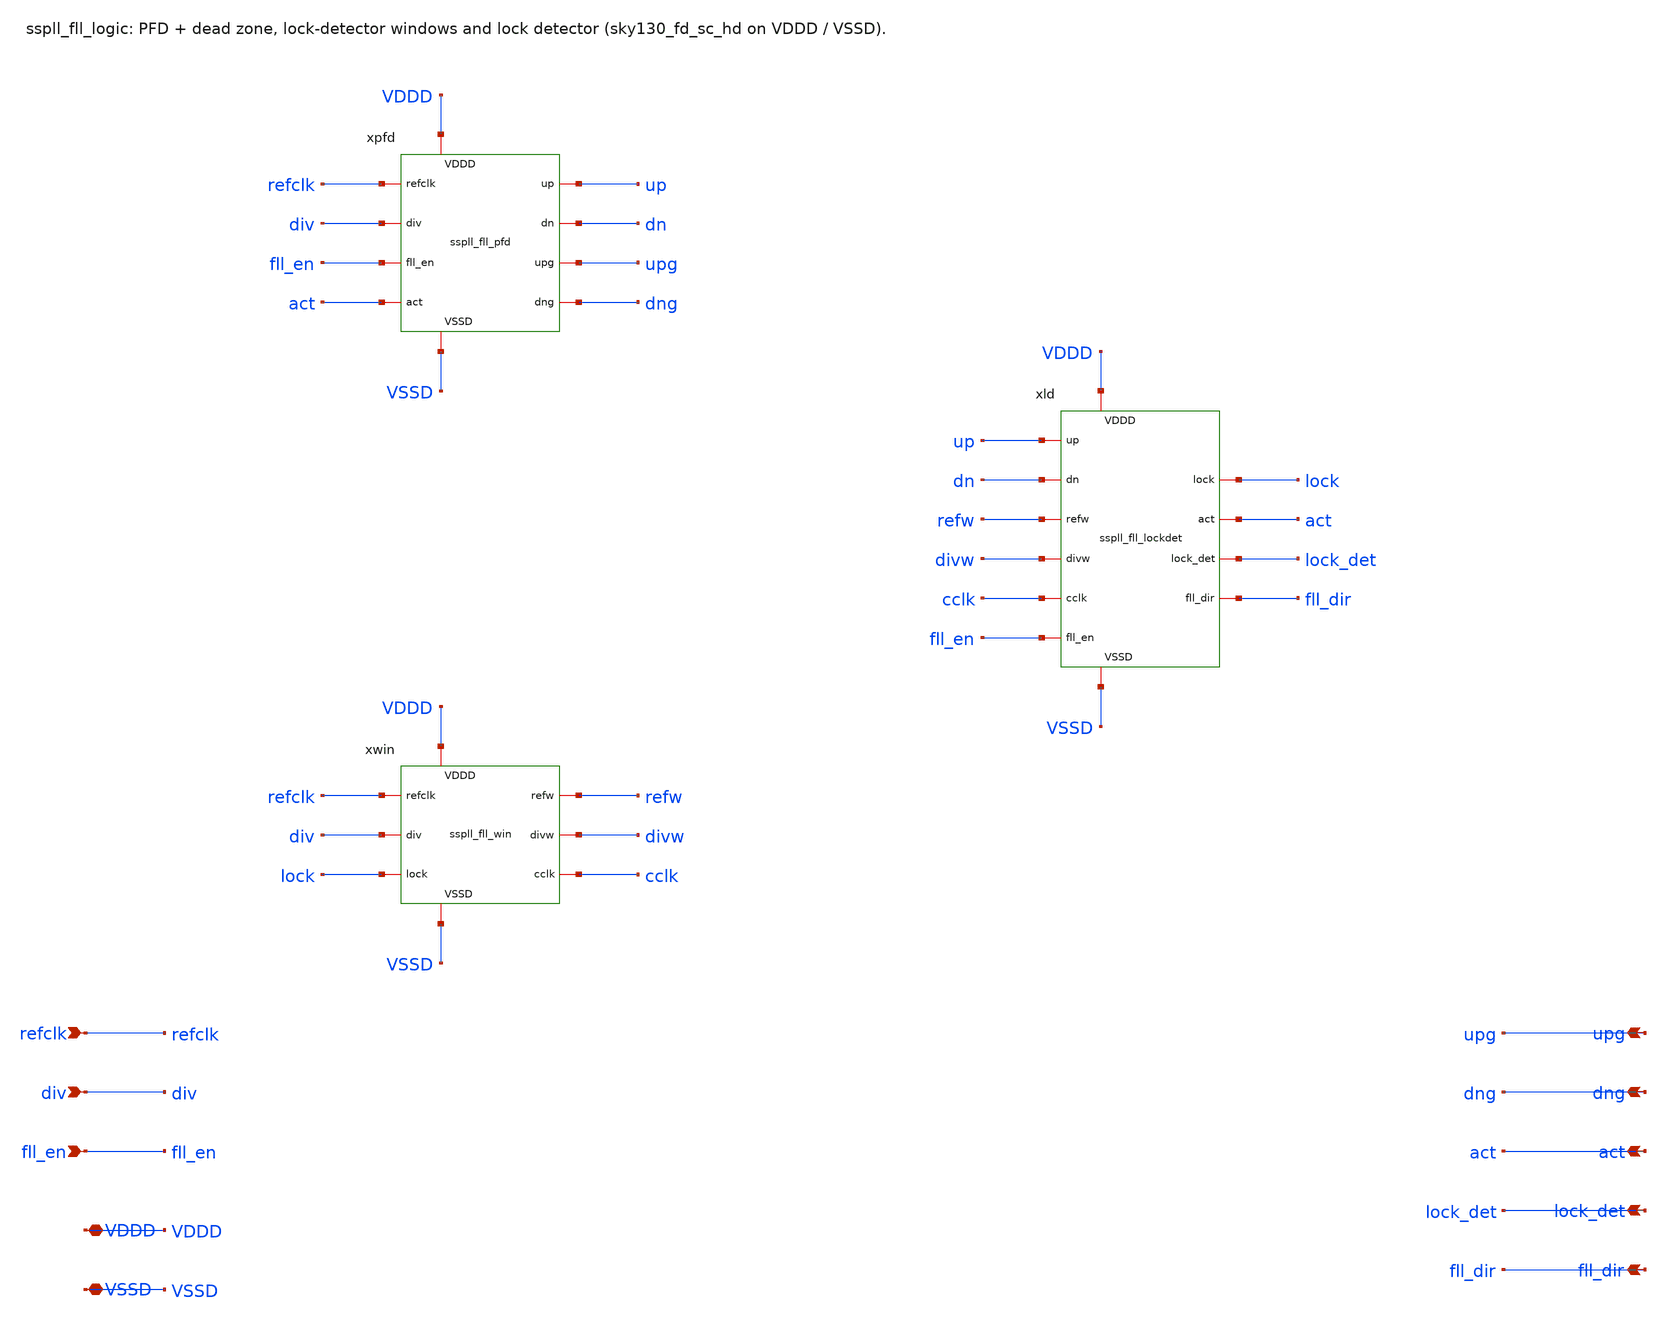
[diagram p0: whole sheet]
** sch_path: xschem/fll_hv/sspll_fll_logic.sch
**.subckt sspll_fll_logic refclk div fll_en upg dng act lock_det fll_dir VDDD VSSD
*.ipin refclk
*.ipin div
*.ipin fll_en
*.opin upg
*.opin dng
*.opin act
*.opin lock_det
*.opin fll_dir
*.iopin VDDD
*.iopin VSSD
xpfd refclk div fll_en act up dn upg dng VDDD VSSD sspll_fll_pfd
xwin refclk div lock refw divw cclk VDDD VSSD sspll_fll_win
xld up dn refw divw cclk fll_en lock act lock_det fll_dir VDDD VSSD sspll_fll_lockdet
**.ends

* expanding   symbol:  sspll_fll_pfd.sym # of pins=10
** sym_path: xschem/fll_hv/sspll_fll_pfd.sym
** sch_path: xschem/fll_hv/sspll_fll_pfd.sch
.subckt sspll_fll_pfd refclk div fll_en act up dn upg dng VDDD VSSD
*.ipin refclk
*.ipin div
*.ipin fll_en
*.ipin act
*.opin up
*.opin dn
*.opin upg
*.opin dng
*.iopin VDDD
*.iopin VSSD
xfu refclk VDDD rb VSSD VSSD VDDD VDDD up sky130_fd_sc_hd__dfrtp_1
xfd div VDDD rb VSSD VSSD VDDD VDDD dn sky130_fd_sc_hd__dfrtp_1
xrn up dn VSSD VSSD VDDD VDDD net1 sky130_fd_sc_hd__nand2_1
xrd net1 VSSD VSSD VDDD VDDD net2 sky130_fd_sc_hd__buf_1
xre net2 fll_en VSSD VSSD VDDD VDDD rb sky130_fd_sc_hd__and2_1
xzu1 up VSSD VSSD VDDD VDDD net3 sky130_fd_sc_hd__clkdlybuf4s25_1
xzu2 net3 VSSD VSSD VDDD VDDD net4 sky130_fd_sc_hd__buf_1
xgu up net4 act VSSD VSSD VDDD VDDD upg sky130_fd_sc_hd__and3_1
xzd1 dn VSSD VSSD VDDD VDDD net5 sky130_fd_sc_hd__clkdlybuf4s25_1
xzd2 net5 VSSD VSSD VDDD VDDD net6 sky130_fd_sc_hd__buf_1
xgd dn net6 act VSSD VSSD VDDD VDDD dng sky130_fd_sc_hd__and3_1
.ends


* expanding   symbol:  sspll_fll_win.sym # of pins=8
** sym_path: xschem/fll_hv/sspll_fll_win.sym
** sch_path: xschem/fll_hv/sspll_fll_win.sch
.subckt sspll_fll_win refclk div lock refw divw cclk VDDD VSSD
*.ipin refclk
*.ipin div
*.ipin lock
*.opin refw
*.opin divw
*.opin cclk
*.iopin VDDD
*.iopin VSSD
xwr1 refclk VSSD VSSD VDDD VDDD net1 sky130_fd_sc_hd__clkdlybuf4s50_1
xwr2 net1 VSSD VSSD VDDD VDDD net2 sky130_fd_sc_hd__clkdlybuf4s50_1
xwr3 net2 VSSD VSSD VDDD VDDD r3 sky130_fd_sc_hd__clkdlybuf4s50_1
xwr4 r3 VSSD VSSD VDDD VDDD net3 sky130_fd_sc_hd__clkdlybuf4s50_1
xwr5 net3 VSSD VSSD VDDD VDDD net4 sky130_fd_sc_hd__clkdlybuf4s50_1
xwr6 net4 VSSD VSSD VDDD VDDD net5 sky130_fd_sc_hd__clkdlybuf4s50_1
xwr7 net5 VSSD VSSD VDDD VDDD r7 sky130_fd_sc_hd__clkdlybuf4s50_1
xwrm r3 r7 lock VSSD VSSD VDDD VDDD refw sky130_fd_sc_hd__mux2_1
xwd1 div VSSD VSSD VDDD VDDD net6 sky130_fd_sc_hd__clkdlybuf4s50_1
xwd2 net6 VSSD VSSD VDDD VDDD net7 sky130_fd_sc_hd__clkdlybuf4s50_1
xwd3 net7 VSSD VSSD VDDD VDDD d3 sky130_fd_sc_hd__clkdlybuf4s50_1
xwd4 d3 VSSD VSSD VDDD VDDD net8 sky130_fd_sc_hd__clkdlybuf4s50_1
xwd5 net8 VSSD VSSD VDDD VDDD net9 sky130_fd_sc_hd__clkdlybuf4s50_1
xwd6 net9 VSSD VSSD VDDD VDDD net10 sky130_fd_sc_hd__clkdlybuf4s50_1
xwd7 net10 VSSD VSSD VDDD VDDD d7 sky130_fd_sc_hd__clkdlybuf4s50_1
xwdm d3 d7 lock VSSD VSSD VDDD VDDD divw sky130_fd_sc_hd__mux2_1
xcc1 r7 VSSD VSSD VDDD VDDD net11 sky130_fd_sc_hd__clkdlybuf4s25_1
xcc2 net11 VSSD VSSD VDDD VDDD cclk sky130_fd_sc_hd__buf_1
.ends


* expanding   symbol:  sspll_fll_lockdet.sym # of pins=12
** sym_path: xschem/fll_hv/sspll_fll_lockdet.sym
** sch_path: xschem/fll_hv/sspll_fll_lockdet.sch
.subckt sspll_fll_lockdet up dn refw divw cclk fll_en lock act lock_det fll_dir VDDD VSSD
*.ipin up
*.ipin dn
*.ipin refw
*.ipin divw
*.ipin cclk
*.ipin fll_en
*.opin lock
*.opin act
*.opin lock_det
*.opin fll_dir
*.iopin VDDD
*.iopin VSSD
xo1 refw up fll_en VSSD VSSD VDDD VDDD o1 sky130_fd_sc_hd__dfrtp_1
xo2 divw dn fll_en VSSD VSSD VDDD VDDD net1 sky130_fd_sc_hd__dfrtp_1
xoo o1 net1 VSSD VSSD VDDD VDDD out sky130_fd_sc_hd__or2_1
xix lock out VSSD VSSD VDDD VDDD inc sky130_fd_sc_hd__xnor2_1
xs0 c0 VSSD VSSD VDDD VDDD s0 sky130_fd_sc_hd__inv_1
xs1 c1 c0 VSSD VSSD VDDD VDDD s1 sky130_fd_sc_hd__xor2_1
xt2 c1 c0 VSSD VSSD VDDD VDDD t2 sky130_fd_sc_hd__and2_1
xs2 c2 t2 VSSD VSSD VDDD VDDD s2 sky130_fd_sc_hd__xor2_1
xt3 c2 c1 c0 VSSD VSSD VDDD VDDD t3 sky130_fd_sc_hd__and3_1
xs3 c3 t3 VSSD VSSD VDDD VDDD s3 sky130_fd_sc_hd__xor2_1
xt4 c3 t3 VSSD VSSD VDDD VDDD t4 sky130_fd_sc_hd__and2_1
xtm t4 t2 lock VSSD VSSD VDDD VDDD term sky130_fd_sc_hd__mux2_1
xtn term VSSD VSSD VDDD VDDD nterm sky130_fd_sc_hd__inv_1
xg inc nterm VSSD VSSD VDDD VDDD g sky130_fd_sc_hd__and2_1
xtg inc term VSSD VSSD VDDD VDDD tg sky130_fd_sc_hd__and2_1
xn0 g s0 VSSD VSSD VDDD VDDD net2 sky130_fd_sc_hd__and2_1
xc0 cclk net2 fll_en VSSD VSSD VDDD VDDD c0 sky130_fd_sc_hd__dfrtp_1
xn1 g s1 VSSD VSSD VDDD VDDD net3 sky130_fd_sc_hd__and2_1
xc1 cclk net3 fll_en VSSD VSSD VDDD VDDD c1 sky130_fd_sc_hd__dfrtp_1
xn2 g s2 VSSD VSSD VDDD VDDD net4 sky130_fd_sc_hd__and2_1
xc2 cclk net4 fll_en VSSD VSSD VDDD VDDD c2 sky130_fd_sc_hd__dfrtp_1
xn3 g s3 VSSD VSSD VDDD VDDD net5 sky130_fd_sc_hd__and2_1
xc3 cclk net5 fll_en VSSD VSSD VDDD VDDD c3 sky130_fd_sc_hd__dfrtp_1
xlx lock tg VSSD VSSD VDDD VDDD net6 sky130_fd_sc_hd__xor2_1
xlf cclk net6 fll_en VSSD VSSD VDDD VDDD lock sky130_fd_sc_hd__dfrtp_1
xli lock VSSD VSSD VDDD VDDD net7 sky130_fd_sc_hd__inv_1
xla fll_en net7 VSSD VSSD VDDD VDDD act sky130_fd_sc_hd__and2_1
xob1 lock VSSD VSSD VDDD VDDD lock_det sky130_fd_sc_hd__buf_1
xob2 o1 VSSD VSSD VDDD VDDD fll_dir sky130_fd_sc_hd__buf_1
.ends

.end
